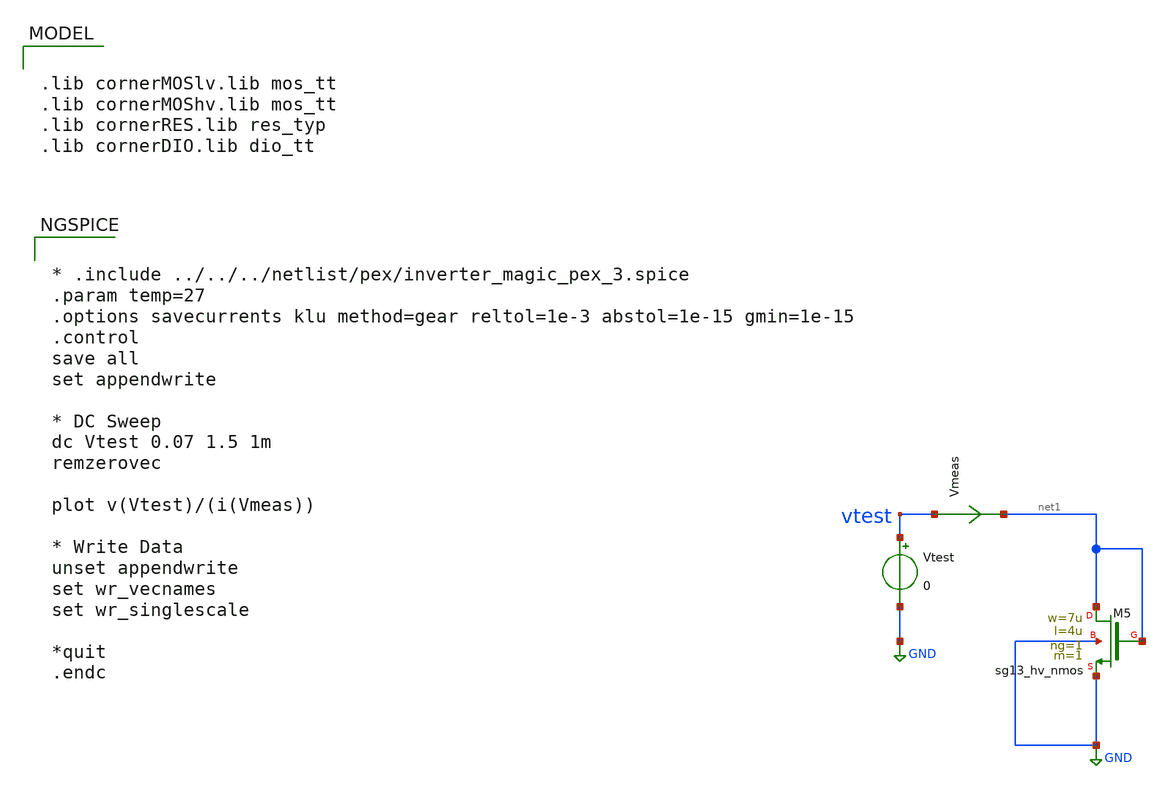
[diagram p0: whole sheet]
** sch_path: macros/heichips26_analog_project/macros/floating-gate/testbenches/xschem/plm.sch
**.subckt plm
XM5 net1 net1 GND GND sg13_hv_nmos w=7u l=4u ng=1 m=1 mm_ok=1
Vmeas vtest net1 0
.save i(vmeas)
Vtest vtest GND 0
**** begin user architecture code


* .include ../../../netlist/pex/inverter_magic_pex_3.spice
.param temp=27
.options savecurrents klu method=gear reltol=1e-3 abstol=1e-15 gmin=1e-15
.control
save all
set appendwrite

* DC Sweep
dc Vtest 0.07 1.5 1m
remzerovec

plot v(Vtest)/(i(Vmeas))

* Write Data
unset appendwrite
set wr_vecnames
set wr_singlescale

*quit
.endc



.lib cornerMOSlv.lib mos_tt
.lib cornerMOShv.lib mos_tt
.lib cornerRES.lib res_typ
.lib cornerDIO.lib dio_tt

**** end user architecture code
**.ends
.GLOBAL GND
.end
